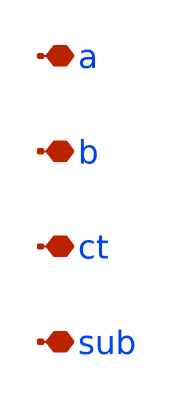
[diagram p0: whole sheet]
** sch_path: sch/inductor/inductor_ind_03_90.sch
**.subckt inductor_ind_03_90 a b ct sub
*.iopin a
*.iopin b
*.iopin ct
*.iopin sub
**** begin user architecture code


R31 net27 b r=1e-2
R26 a net23 r=1e-2
C24 net35 net27 c=8.337e-15
C25 net23 net37 c=53.8e-15
C0 net27 net31 c=53.8e-15
R1 sub net31 r=21.56
R13 net23 net35 r=50.11
R10 sub net37 r=21.56
R0 net41 net27 r=1.019
R9 net23 net39 r=1.019
L0 net39 ct l=760.5e-12
L1 ct net41 l=760.5e-12


**** end user architecture code
**.ends
.end
